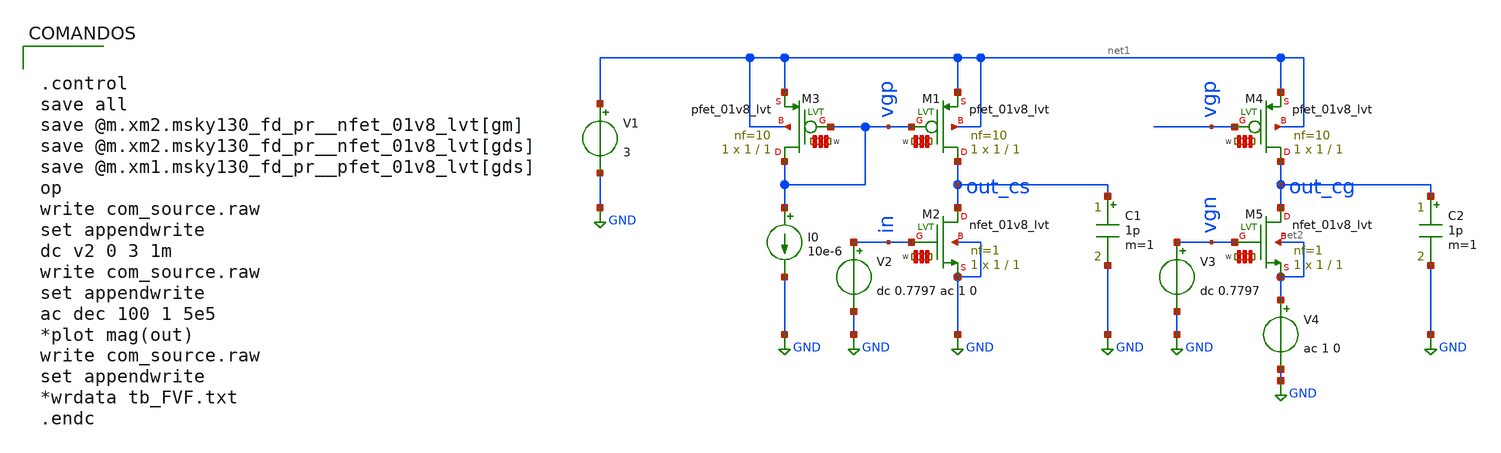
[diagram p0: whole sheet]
** sch_path: com_source.sch
**.subckt com_source
I0 vgp GND 10e-6
V1 net1 GND 3
V2 in GND dc 0.7797 ac 1 0
XM1 out_cs vgp net1 net1 sky130_fd_pr__pfet_01v8_lvt L=1 W='1 * 10 ' nf=10 ad='int((nf+1)/2) * W / nf * 0.29'
+ as='int((nf+2)/2) * W / nf * 0.29' pd='2*int((nf+1)/2) * (W / nf + 0.29)' ps='2*int((nf+2)/2) * (W / nf + 0.29)'
+ nrd='0.29 / W ' nrs='0.29 / W ' sa=0 sb=0 sd=0 mult=1 m=1
XM3 vgp vgp net1 net1 sky130_fd_pr__pfet_01v8_lvt L=1 W='1 * 10 ' nf=10 ad='int((nf+1)/2) * W / nf * 0.29'
+ as='int((nf+2)/2) * W / nf * 0.29' pd='2*int((nf+1)/2) * (W / nf + 0.29)' ps='2*int((nf+2)/2) * (W / nf + 0.29)'
+ nrd='0.29 / W ' nrs='0.29 / W ' sa=0 sb=0 sd=0 mult=1 m=1
XM2 out_cs in GND GND sky130_fd_pr__nfet_01v8_lvt L=1 W='1 * 1 ' nf=1 ad='int((nf+1)/2) * W / nf * 0.29'
+ as='int((nf+2)/2) * W / nf * 0.29' pd='2*int((nf+1)/2) * (W / nf + 0.29)' ps='2*int((nf+2)/2) * (W / nf + 0.29)'
+ nrd='0.29 / W ' nrs='0.29 / W ' sa=0 sb=0 sd=0 mult=1 m=1
C1 out_cs GND 1p m=1
V3 vgn GND dc 0.7797
XM4 out_cg vgp net1 net1 sky130_fd_pr__pfet_01v8_lvt L=1 W='1 * 10 ' nf=10 ad='int((nf+1)/2) * W / nf * 0.29'
+ as='int((nf+2)/2) * W / nf * 0.29' pd='2*int((nf+1)/2) * (W / nf + 0.29)' ps='2*int((nf+2)/2) * (W / nf + 0.29)'
+ nrd='0.29 / W ' nrs='0.29 / W ' sa=0 sb=0 sd=0 mult=1 m=1
XM5 out_cg vgn net2 net2 sky130_fd_pr__nfet_01v8_lvt L=1 W='1 * 1 ' nf=1 ad='int((nf+1)/2) * W / nf * 0.29'
+ as='int((nf+2)/2) * W / nf * 0.29' pd='2*int((nf+1)/2) * (W / nf + 0.29)' ps='2*int((nf+2)/2) * (W / nf + 0.29)'
+ nrd='0.29 / W ' nrs='0.29 / W ' sa=0 sb=0 sd=0 mult=1 m=1
C2 out_cg GND 1p m=1
V4 net2 GND ac 1 0
**** begin user architecture code

** opencircuitdesign pdks install
.lib $::SKYWATER_MODELS/sky130.lib.spice tt




.control
save all
save @m.xm2.msky130_fd_pr__nfet_01v8_lvt[gm]
save @m.xm2.msky130_fd_pr__nfet_01v8_lvt[gds]
save @m.xm1.msky130_fd_pr__pfet_01v8_lvt[gds]
op
write com_source.raw
set appendwrite
dc v2 0 3 1m
write com_source.raw
set appendwrite
ac dec 100 1 5e5
*plot mag(out)
write com_source.raw
set appendwrite
*wrdata tb_FVF.txt
.endc


**** end user architecture code
**.ends
.GLOBAL GND
.end
